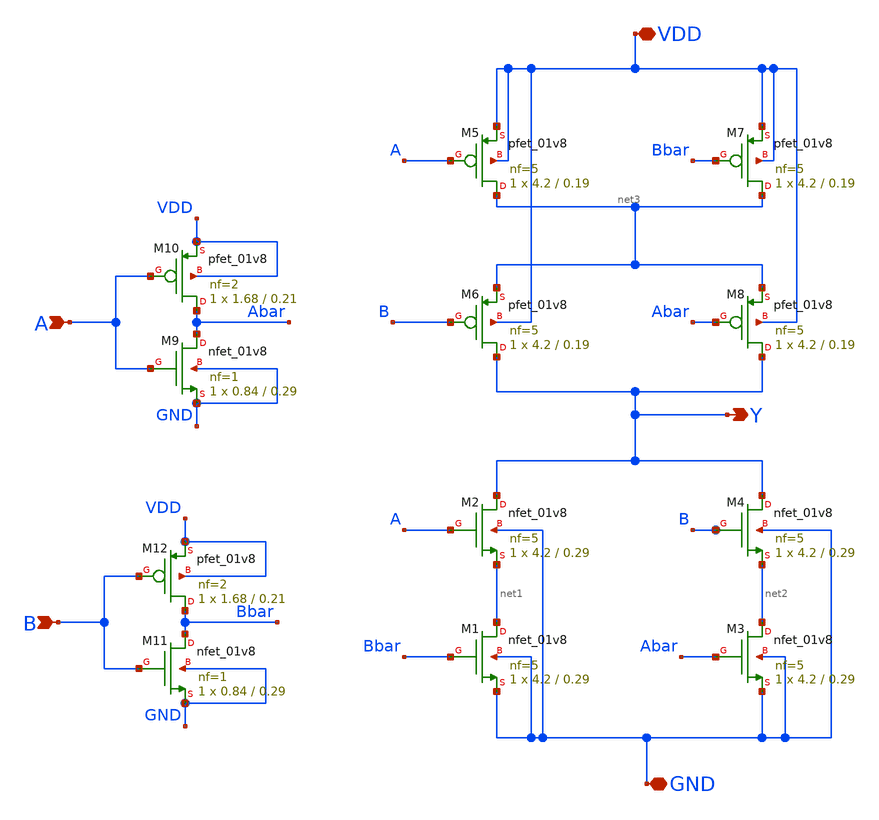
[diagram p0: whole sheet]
** sch_path: cells/XNOR2X4/schematic/xnor2x4.sch
**.subckt xnor2x4 A B Y VDD GND
*.ipin A
*.ipin B
*.opin Y
*.iopin VDD
*.iopin GND
XM9 Abar A GND GND sky130_fd_pr__nfet_01v8 L=0.29 W=0.84 nf=1 ad='int((1 + 1)/2) * 0.84 / 1 * 0.29' as='int((1 + 2)/2) * 0.84 / 1 * 0.29'
+ pd='2*int((1 + 1)/2) * (0.84 / 1 + 0.29)' ps='2*int((1 + 2)/2) * (0.84 / 1 + 0.29)' nrd='0.29 / 0.84 '
+ nrs='0.29 / 0.84 ' sa=0 sb=0 sd=0 mult=1 m=1
XM10 Abar A VDD VDD sky130_fd_pr__pfet_01v8 L=0.21 W=1.68 nf=2 ad='int((2 + 1)/2) * 1.68 / 2 * 0.29'
+ as='int((2 + 2)/2) * 1.68 / 2 * 0.29' pd='2*int((2 + 1)/2) * (1.68 / 2 + 0.29)' ps='2*int((2 + 2)/2) * (1.68 / 2 + 0.29)'
+ nrd='0.29 / 1.68 ' nrs='0.29 / 1.68 ' sa=0 sb=0 sd=0 mult=1 m=1
XM2 Y A net1 GND sky130_fd_pr__nfet_01v8 L=0.29 W=4.2 nf=5 ad='int((5 + 1)/2) * 4.2 / 5 * 0.29' as='int((5 + 2)/2) * 4.2 / 5 * 0.29'
+ pd='2*int((5 + 1)/2) * (4.2 / 5 + 0.29)' ps='2*int((5 + 2)/2) * (4.2 / 5 + 0.29)' nrd='0.29 / 4.2 ' nrs='0.29 / 4.2 '
+ sa=0 sb=0 sd=0 mult=1 m=1
XM5 net3 A VDD VDD sky130_fd_pr__pfet_01v8 L=0.19 W=4.2 nf=5 ad='int((5 + 1)/2) * 4.2 / 5 * 0.29' as='int((5 + 2)/2) * 4.2 / 5 * 0.29'
+ pd='2*int((5 + 1)/2) * (4.2 / 5 + 0.29)' ps='2*int((5 + 2)/2) * (4.2 / 5 + 0.29)' nrd='0.29 / 4.2 ' nrs='0.29 / 4.2 '
+ sa=0 sb=0 sd=0 mult=1 m=1
XM12 Bbar B VDD VDD sky130_fd_pr__pfet_01v8 L=0.21 W=1.68 nf=2 ad='int((2 + 1)/2) * 1.68 / 2 * 0.29'
+ as='int((2 + 2)/2) * 1.68 / 2 * 0.29' pd='2*int((2 + 1)/2) * (1.68 / 2 + 0.29)' ps='2*int((2 + 2)/2) * (1.68 / 2 + 0.29)'
+ nrd='0.29 / 1.68 ' nrs='0.29 / 1.68 ' sa=0 sb=0 sd=0 mult=1 m=1
XM11 Bbar B GND GND sky130_fd_pr__nfet_01v8 L=0.29 W=0.84 nf=1 ad='int((1 + 1)/2) * 0.84 / 1 * 0.29'
+ as='int((1 + 2)/2) * 0.84 / 1 * 0.29' pd='2*int((1 + 1)/2) * (0.84 / 1 + 0.29)' ps='2*int((1 + 2)/2) * (0.84 / 1 + 0.29)'
+ nrd='0.29 / 0.84 ' nrs='0.29 / 0.84 ' sa=0 sb=0 sd=0 mult=1 m=1
XM1 net1 Bbar GND GND sky130_fd_pr__nfet_01v8 L=0.29 W=4.2 nf=5 ad='int((5 + 1)/2) * 4.2 / 5 * 0.29'
+ as='int((5 + 2)/2) * 4.2 / 5 * 0.29' pd='2*int((5 + 1)/2) * (4.2 / 5 + 0.29)' ps='2*int((5 + 2)/2) * (4.2 / 5 + 0.29)'
+ nrd='0.29 / 4.2 ' nrs='0.29 / 4.2 ' sa=0 sb=0 sd=0 mult=1 m=1
XM3 net2 Abar GND GND sky130_fd_pr__nfet_01v8 L=0.29 W=4.2 nf=5 ad='int((5 + 1)/2) * 4.2 / 5 * 0.29'
+ as='int((5 + 2)/2) * 4.2 / 5 * 0.29' pd='2*int((5 + 1)/2) * (4.2 / 5 + 0.29)' ps='2*int((5 + 2)/2) * (4.2 / 5 + 0.29)'
+ nrd='0.29 / 4.2 ' nrs='0.29 / 4.2 ' sa=0 sb=0 sd=0 mult=1 m=1
XM4 Y B net2 GND sky130_fd_pr__nfet_01v8 L=0.29 W=4.2 nf=5 ad='int((5 + 1)/2) * 4.2 / 5 * 0.29' as='int((5 + 2)/2) * 4.2 / 5 * 0.29'
+ pd='2*int((5 + 1)/2) * (4.2 / 5 + 0.29)' ps='2*int((5 + 2)/2) * (4.2 / 5 + 0.29)' nrd='0.29 / 4.2 ' nrs='0.29 / 4.2 '
+ sa=0 sb=0 sd=0 mult=1 m=1
XM6 Y B net3 VDD sky130_fd_pr__pfet_01v8 L=0.19 W=4.2 nf=5 ad='int((5 + 1)/2) * 4.2 / 5 * 0.29' as='int((5 + 2)/2) * 4.2 / 5 * 0.29'
+ pd='2*int((5 + 1)/2) * (4.2 / 5 + 0.29)' ps='2*int((5 + 2)/2) * (4.2 / 5 + 0.29)' nrd='0.29 / 4.2 ' nrs='0.29 / 4.2 '
+ sa=0 sb=0 sd=0 mult=1 m=1
XM8 Y Abar net3 VDD sky130_fd_pr__pfet_01v8 L=0.19 W=4.2 nf=5 ad='int((5 + 1)/2) * 4.2 / 5 * 0.29' as='int((5 + 2)/2) * 4.2 / 5 * 0.29'
+ pd='2*int((5 + 1)/2) * (4.2 / 5 + 0.29)' ps='2*int((5 + 2)/2) * (4.2 / 5 + 0.29)' nrd='0.29 / 4.2 ' nrs='0.29 / 4.2 '
+ sa=0 sb=0 sd=0 mult=1 m=1
XM7 net3 Bbar VDD VDD sky130_fd_pr__pfet_01v8 L=0.19 W=4.2 nf=5 ad='int((5 + 1)/2) * 4.2 / 5 * 0.29'
+ as='int((5 + 2)/2) * 4.2 / 5 * 0.29' pd='2*int((5 + 1)/2) * (4.2 / 5 + 0.29)' ps='2*int((5 + 2)/2) * (4.2 / 5 + 0.29)'
+ nrd='0.29 / 4.2 ' nrs='0.29 / 4.2 ' sa=0 sb=0 sd=0 mult=1 m=1
**.ends
.end
